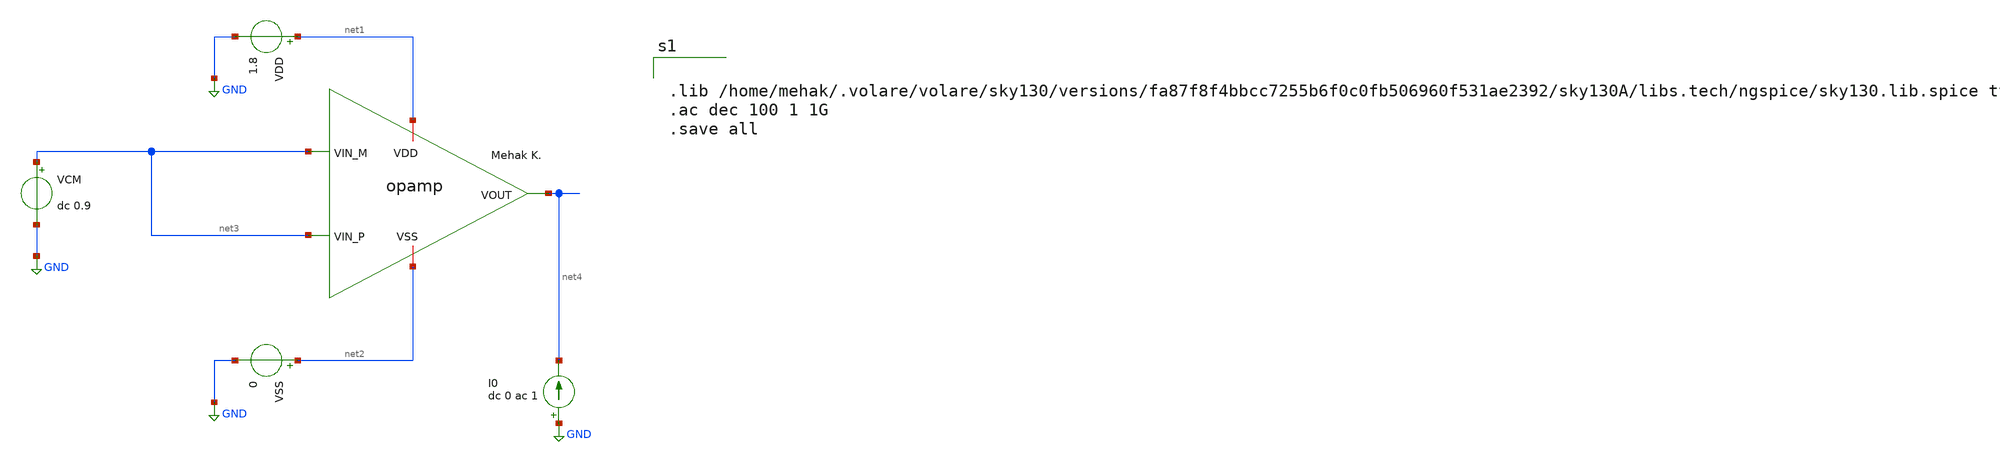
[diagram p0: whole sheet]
** sch_path: analog/build/schematic/tb_impedance.sch
**.subckt tb_impedance
VDD net1 GND 1.8
VSS net2 GND 0
x1 net1 net4 net3 net3 net2 opamp_two_stage
I0 GND net4 dc 0 ac 1
VCM net3 GND dc 0.9
**** begin user architecture code


.lib /home/mehak/.volare/volare/sky130/versions/fa87f8f4bbcc7255b6f0c0fb506960f531ae2392/sky130A/libs.tech/ngspice/sky130.lib.spice tt
.ac dec 100 1 1G
.save all


**** end user architecture code
**.ends
.GLOBAL GND
.end
